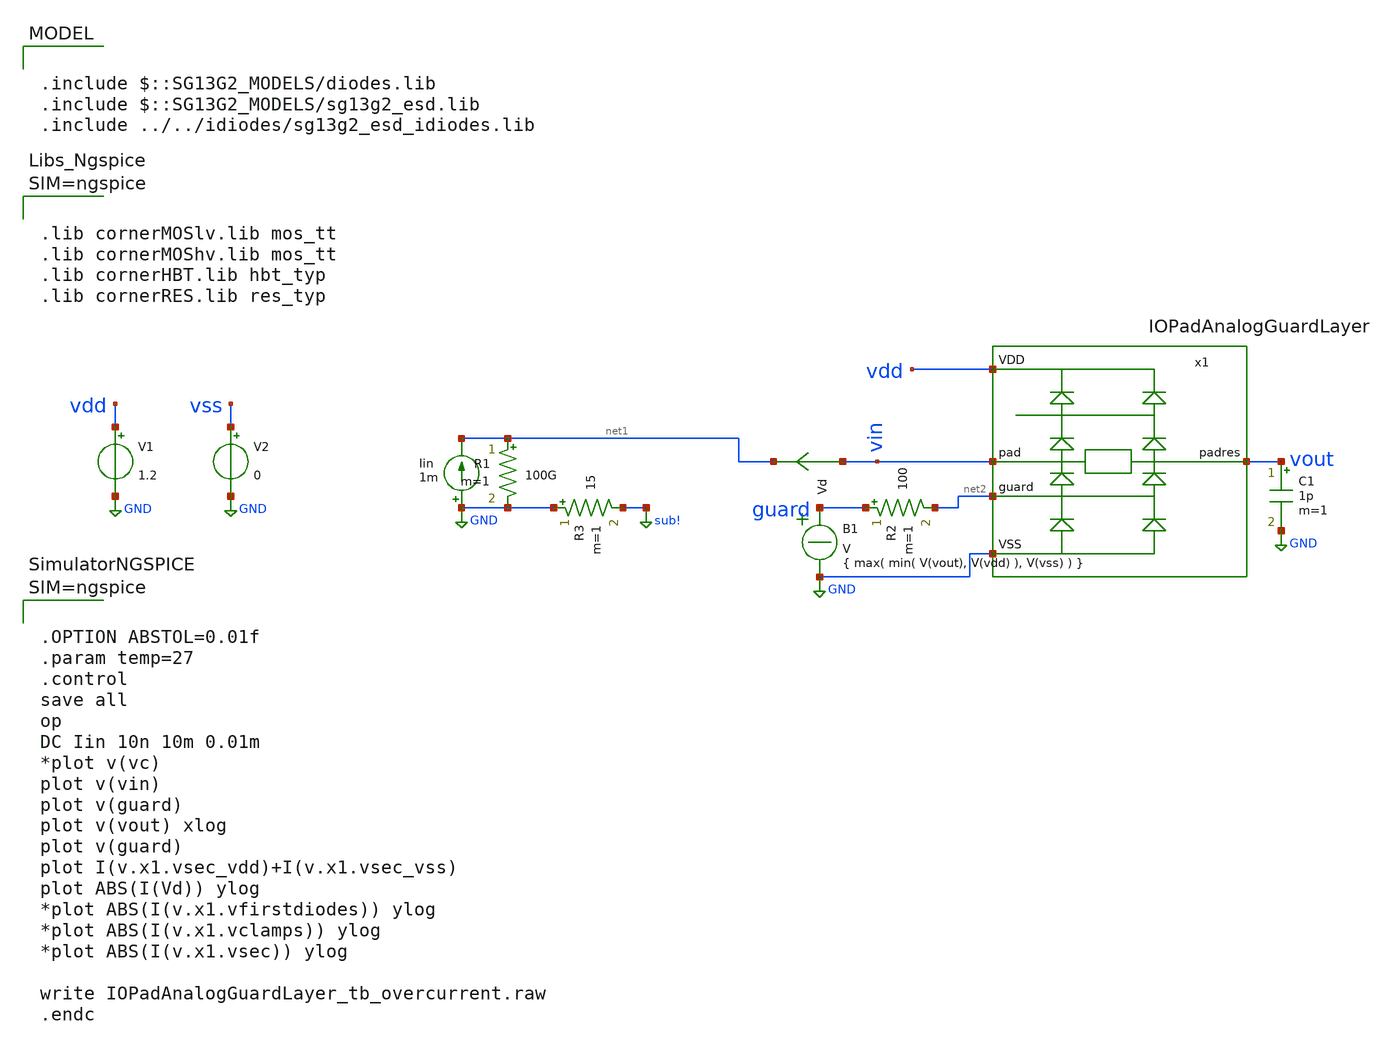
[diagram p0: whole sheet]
** sch_path: trident_test_structures/design_data/xschem/IOPadAnalogGuardLayer/IOPadAnalogGuardLayer_tb_overcurrent.sch
**.subckt IOPadAnalogGuardLayer_tb_overcurrent
V1 vdd GND 1.2
Vd vin net1 0
.save i(vd)
C1 vout GND 1p m=1
R2 guard net2 100 m=1
R3 GND sub! 15 m=1
x1 vdd vin vout net2 GND IOPadAnalogGuardLayer
Iin GND net1 1m
R1 net1 GND 100G m=1
V2 vss GND 0
B1 guard GND V = { max( min( V(vout), V(vdd) ), V(vss) ) }
**** begin user architecture code



.lib cornerMOSlv.lib mos_tt
.lib cornerMOShv.lib mos_tt
.lib cornerHBT.lib hbt_typ
.lib cornerRES.lib res_typ






.OPTION ABSTOL=0.01f
.param temp=27
.control
save all
op
DC Iin 10n 10m 0.01m
*plot v(vc)
plot v(vin)
plot v(guard)
plot v(vout) xlog
plot v(guard)
plot I(v.x1.vsec_vdd)+I(v.x1.vsec_vss)
plot ABS(I(Vd)) ylog
*plot ABS(I(v.x1.vfirstdiodes)) ylog
*plot ABS(I(v.x1.vclamps)) ylog
*plot ABS(I(v.x1.vsec)) ylog

write IOPadAnalogGuardLayer_tb_overcurrent.raw
.endc




.include $::SG13G2_MODELS/diodes.lib
.include $::SG13G2_MODELS/sg13g2_esd.lib
.include ../../idiodes/sg13g2_esd_idiodes.lib

**** end user architecture code
**.ends
.GLOBAL GND
.GLOBAL sub!
.end
